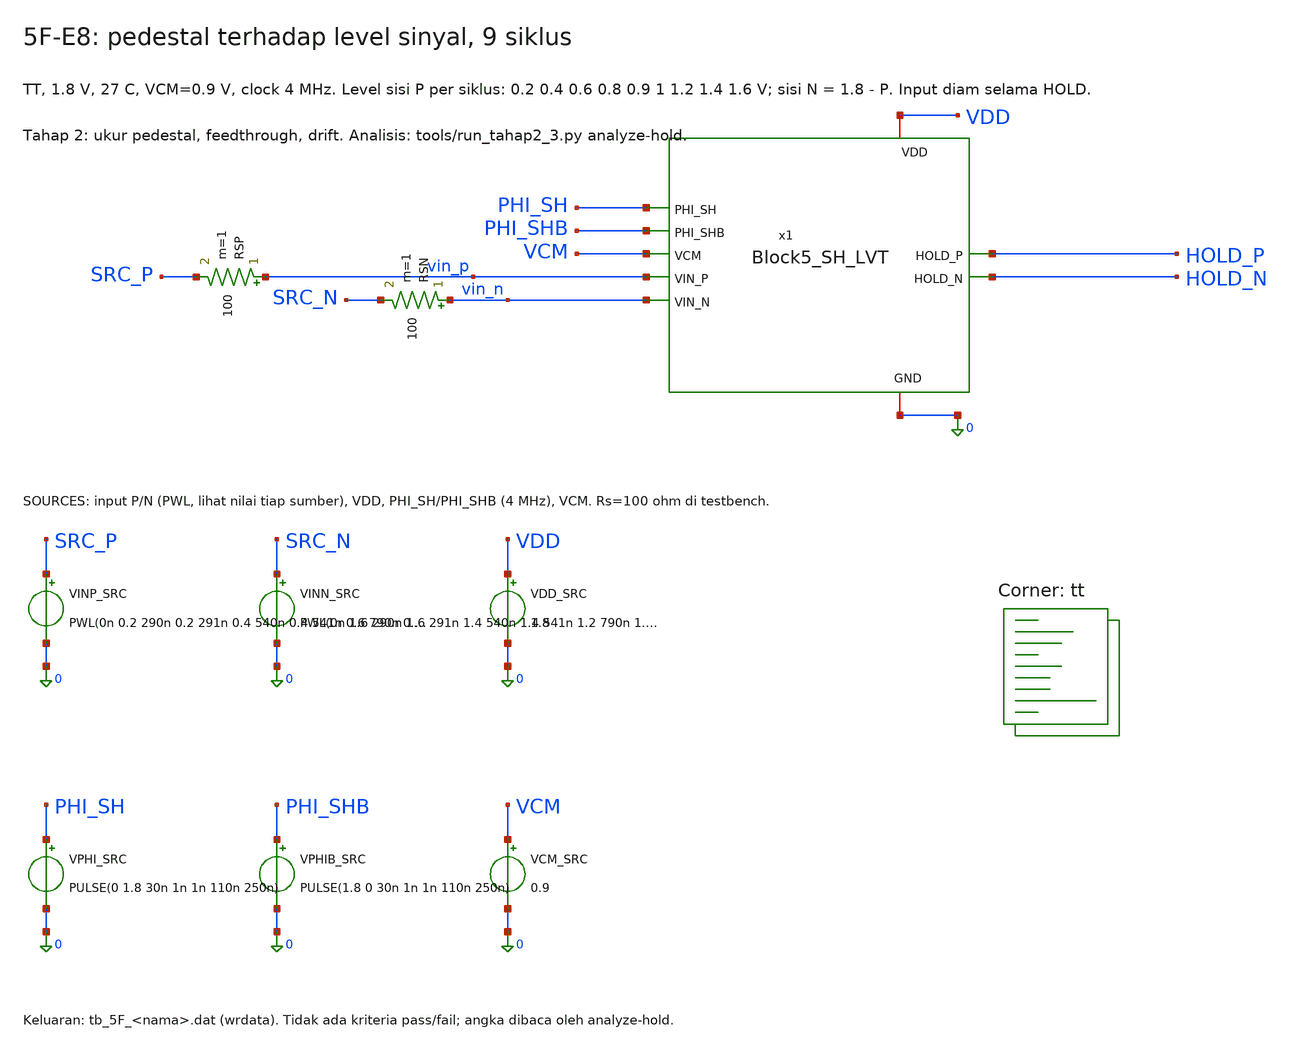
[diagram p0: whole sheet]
** sch_path: blocks/05_Switch_Network/sim/tb_5F_E8_level_sweep.sch
**.subckt tb_5F_E8_level_sweep
RSP vin_p SRC_P 100 m=1
RSN vin_n SRC_N 100 m=1
VINP_SRC SRC_P 0 PWL(0n 0.2 290n 0.2 291n 0.4 540n 0.4 541n 0.6 790n 0.6 791n 0.8 1040n 0.8 1041n
+ 0.9 1290n 0.9 1291n 1 1540n 1 1541n 1.2 1790n 1.2 1791n 1.4 2040n 1.4 2041n 1.6 2450n 1.6)
VINN_SRC SRC_N 0 PWL(0n 1.6 290n 1.6 291n 1.4 540n 1.4 541n 1.2 790n 1.2 791n 1 1040n 1 1041n 0.9
+ 1290n 0.9 1291n 0.8 1540n 0.8 1541n 0.6 1790n 0.6 1791n 0.4 2040n 0.4 2041n 0.2 2450n 0.2)
VDD_SRC VDD 0 1.8
VPHI_SRC PHI_SH 0 PULSE(0 1.8 30n 1n 1n 110n 250n)
VPHIB_SRC PHI_SHB 0 PULSE(1.8 0 30n 1n 1n 110n 250n)
VCM_SRC VCM 0 0.9
x1 VDD PHI_SH PHI_SHB 0 VCM vin_p HOLD_P HOLD_N vin_n Block5_SH_LVT
**** begin user architecture code
.lib $::SKYWATER_MODELS/sky130.lib.spice tt


* E8_level_sweep: diagnosa hold error Block 5 (tahap 2). TT, 1.8 V, 27 C.
* .ic hanya kondisi awal numerik, bukan rangkaian reset.
.option scale=1e-6 reltol=1e-5 abstol=1e-15 vntol=1e-8
.temp 27
.ic V(HOLD_P)=0.9 V(HOLD_N)=0.9
.control
save all
set wr_singlescale
set wr_vecnames
set numdgt=15
tran 0.1n 2350n 0 0.1n
wrdata tb_5F_E8_level_sweep.dat v(SRC_P) v(SRC_N) v(VIN_P) v(VIN_N) v(HOLD_P) v(HOLD_N) v(PHI_SH)
+ v(PHI_SHB)
echo TB_5F_DONE
.endc


**** end user architecture code
**.ends

* expanding   symbol:  blocks/05_Switch_Network/xschem/Block5_SH_LVT.sym # of pins=9
** sym_path: blocks/05_Switch_Network/xschem/Block5_SH_LVT.sym
** sch_path: blocks/05_Switch_Network/xschem/Block5_SH_LVT.sch
.subckt Block5_SH_LVT VDD PHI_SH PHI_SHB GND VCM VIN_P HOLD_P HOLD_N VIN_N
*.ipin VIN_P
*.ipin VIN_N
*.ipin PHI_SH
*.ipin PHI_SHB
*.iopin VDD
*.iopin GND
*.ipin VCM
*.opin HOLD_P
*.opin HOLD_N
CH_P HOLD_P VCM 1p m=1
CH_N HOLD_N VCM 1p m=1
x3 VIN_P HOLD_P PHI_SHB PHI_SH VDD GND TG_SC_LVT
x1 VIN_N HOLD_N PHI_SHB PHI_SH VDD GND TG_SC_LVT
.ends


* expanding   symbol:  blocks/05_Switch_Network/xschem/TG_SC_LVT.sym # of pins=6
** sym_path: blocks/05_Switch_Network/xschem/TG_SC_LVT.sym
** sch_path: blocks/05_Switch_Network/xschem/TG_SC_LVT.sch
.subckt TG_SC_LVT A B CLK_P CLK_N VDD GND
*.iopin A
*.iopin B
*.ipin CLK_P
*.ipin CLK_N
*.iopin VDD
*.iopin GND
XMP A CLK_P B VDD sky130_fd_pr__pfet_01v8_lvt L=0.35 W=8 nf=1 ad='int((1 + 1)/2) * 8 / 1 * 0.29' as='int((1 + 2)/2) * 8 / 1 * 0.29'
+ pd='2*int((1 + 1)/2) * (8 / 1 + 0.29)' ps='2*int((1 + 2)/2) * (8 / 1 + 0.29)' nrd='0.29 / 8 ' nrs='0.29 / 8 '
+ sa=0 sb=0 sd=0 mult=1
XMN A CLK_N B GND sky130_fd_pr__nfet_01v8_lvt L=0.15 W=4 nf=1 ad='int((1 + 1)/2) * 4 / 1 * 0.29' as='int((1 + 2)/2) * 4 / 1 * 0.29'
+ pd='2*int((1 + 1)/2) * (4 / 1 + 0.29)' ps='2*int((1 + 2)/2) * (4 / 1 + 0.29)' nrd='0.29 / 4 ' nrs='0.29 / 4 '
+ sa=0 sb=0 sd=0 mult=1
.ends

.end
